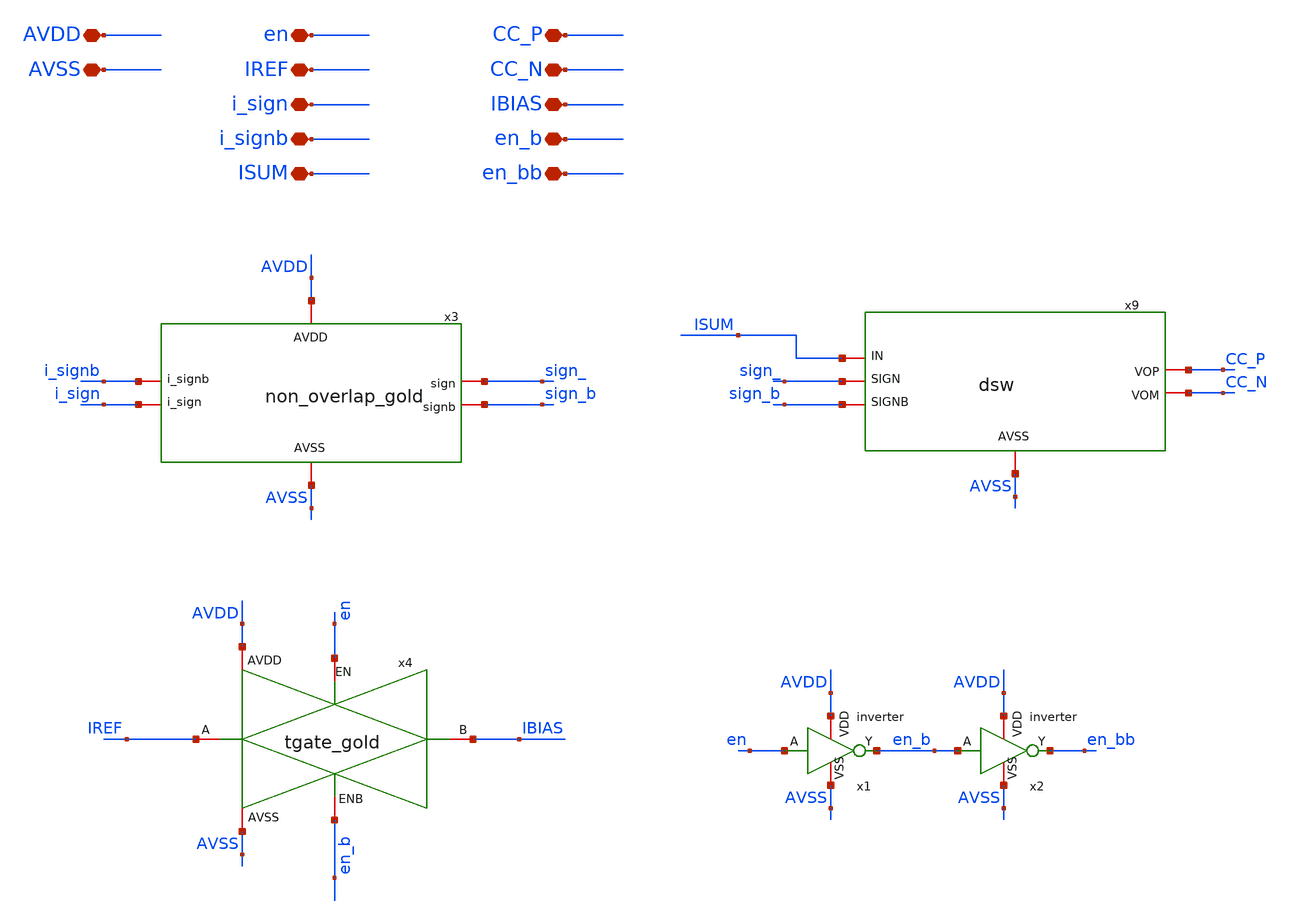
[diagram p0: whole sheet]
** sch_path: current_generator/analog/DAC/schematics/sub_top_gold.sch
**.subckt sub_top_gold AVDD AVSS en en_b en_bb i_sign i_signb ISUM CC_P CC_N IREF IBIAS
*.iopin AVDD
*.iopin AVSS
*.iopin en
*.iopin en_b
*.iopin en_bb
*.iopin i_sign
*.iopin i_signb
*.iopin ISUM
*.iopin CC_P
*.iopin CC_N
*.iopin IREF
*.iopin IBIAS
x9 sign_ sign_b ISUM AVSS CC_P CC_N dsw
x1 en en_b AVDD AVSS inverter
x2 en_b en_bb AVDD AVSS inverter
x3 AVDD AVSS i_sign i_signb sign_ sign_b non_overlap_gold
x4 AVDD AVSS en en_b IREF IBIAS tgate_gold
**.ends
.end
